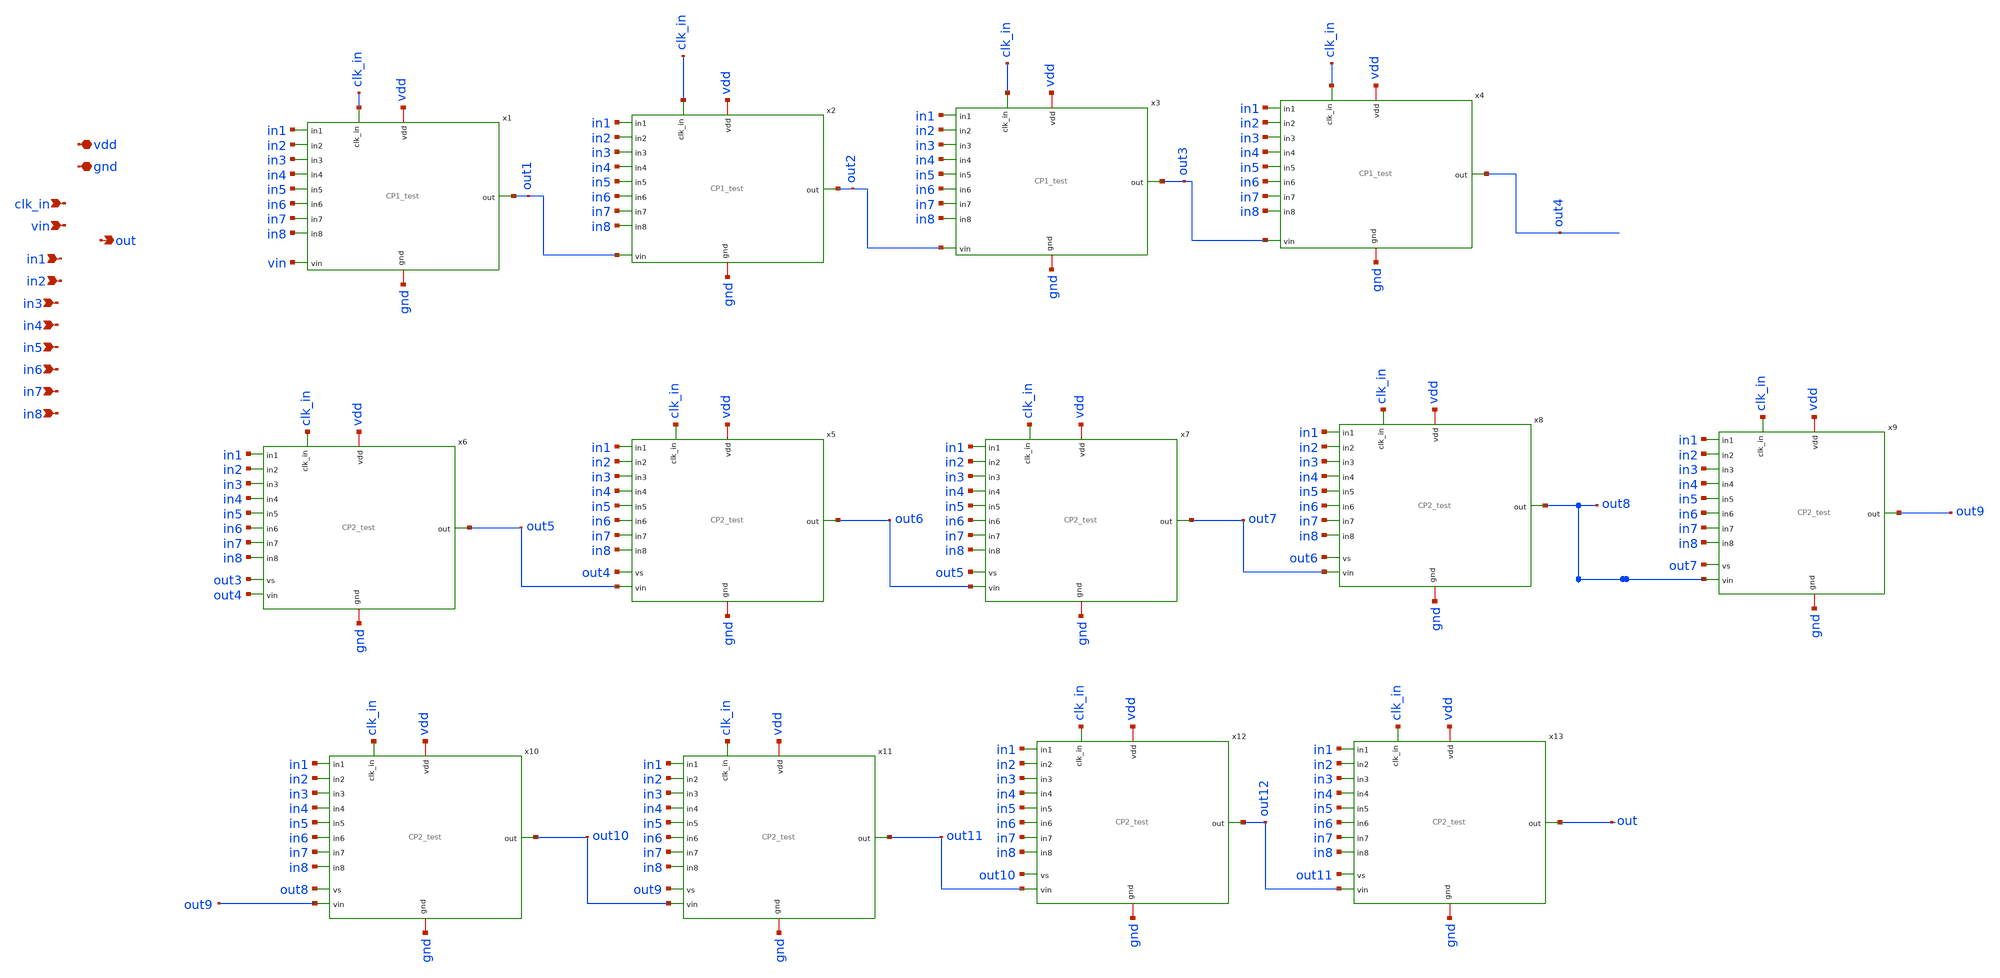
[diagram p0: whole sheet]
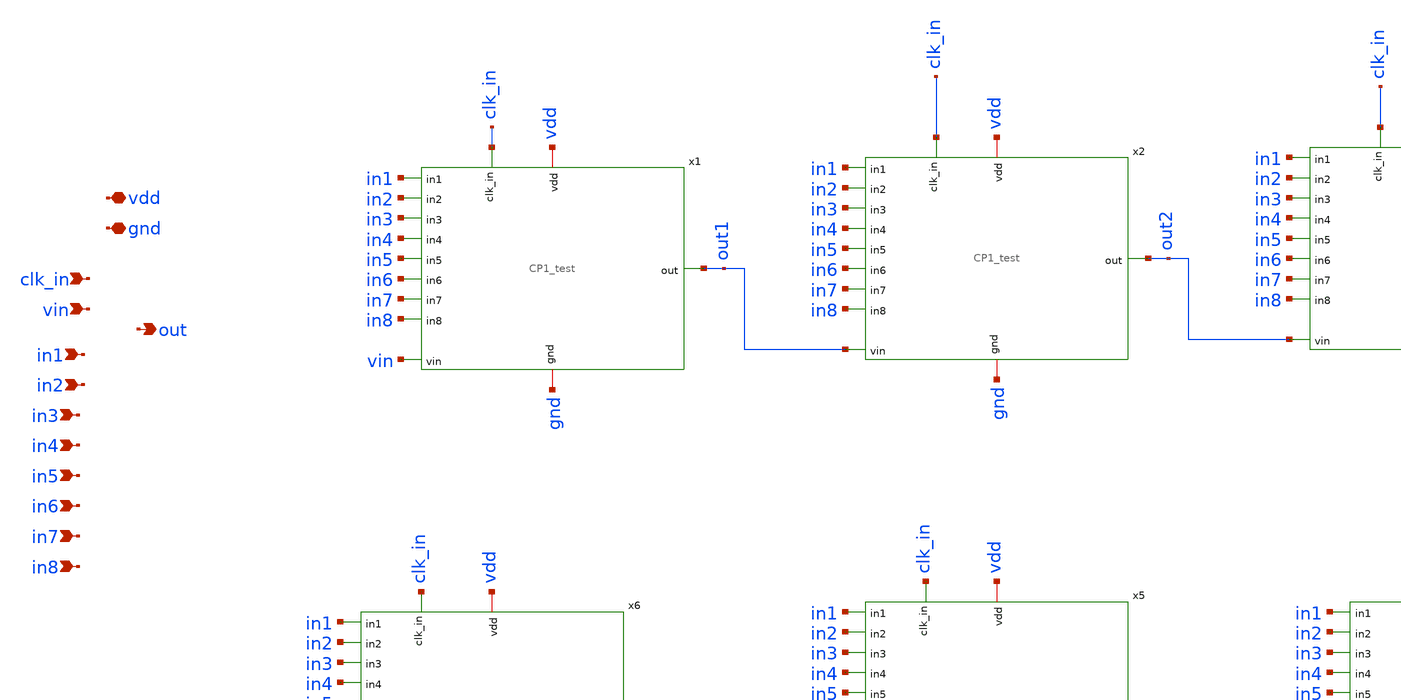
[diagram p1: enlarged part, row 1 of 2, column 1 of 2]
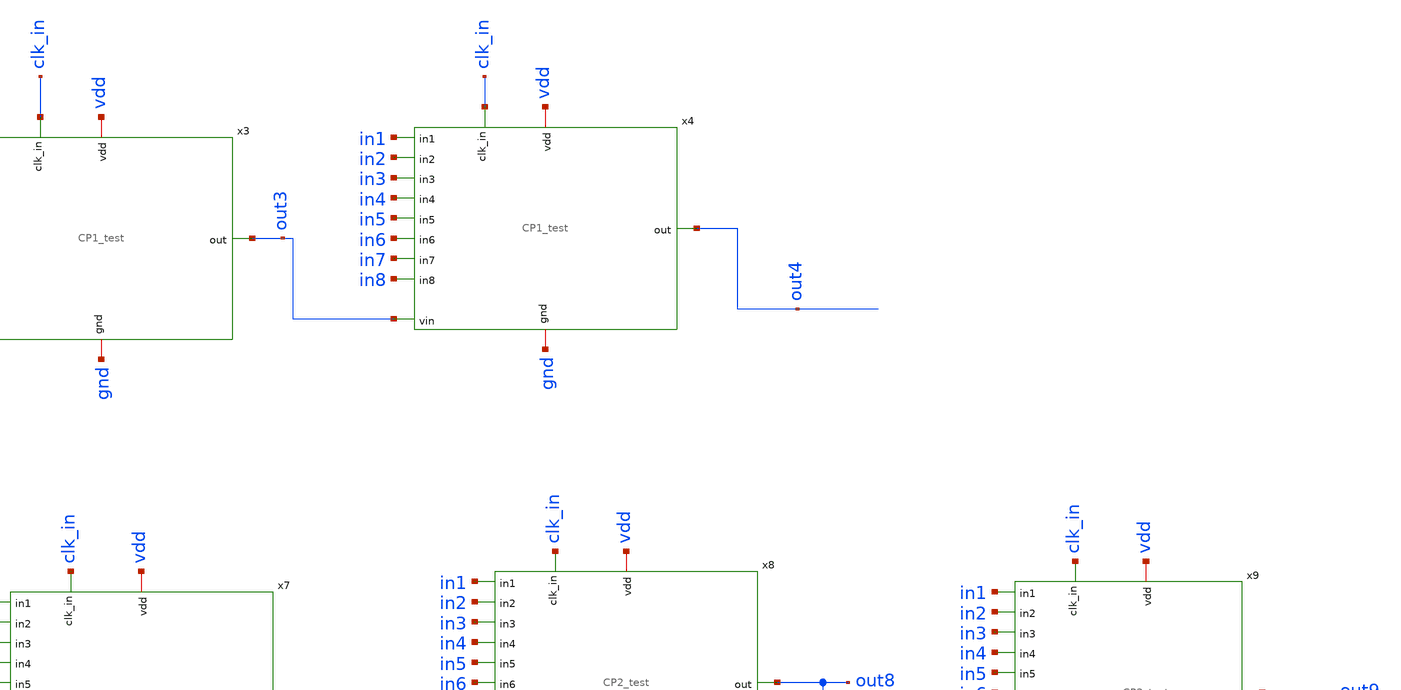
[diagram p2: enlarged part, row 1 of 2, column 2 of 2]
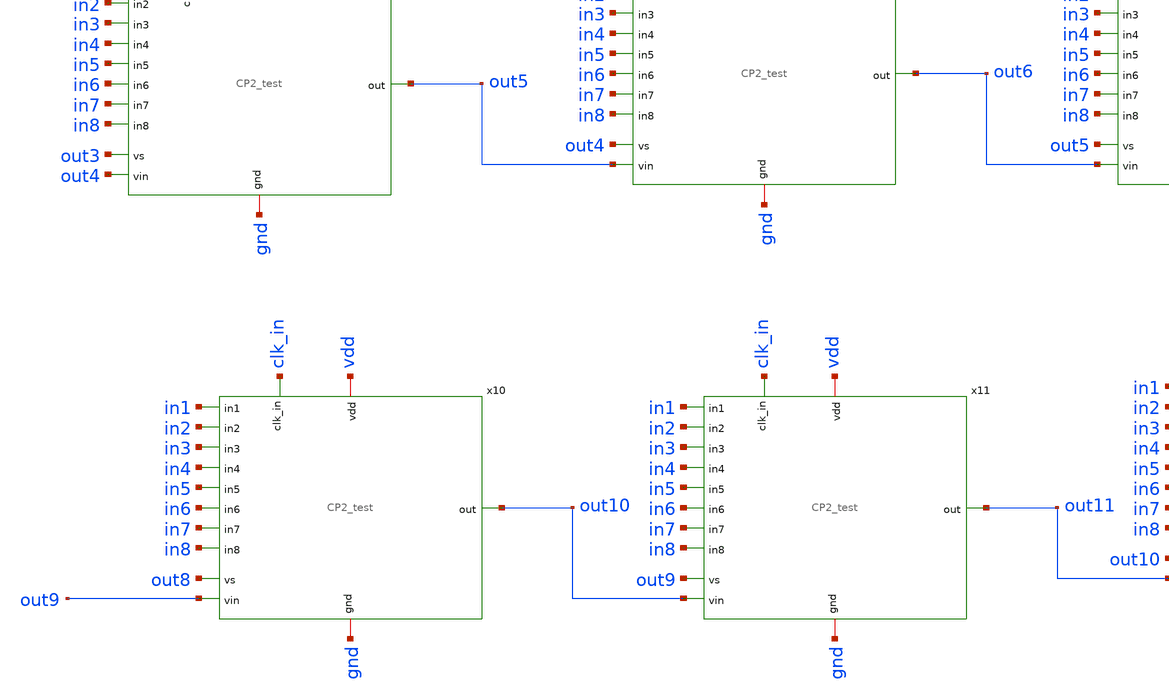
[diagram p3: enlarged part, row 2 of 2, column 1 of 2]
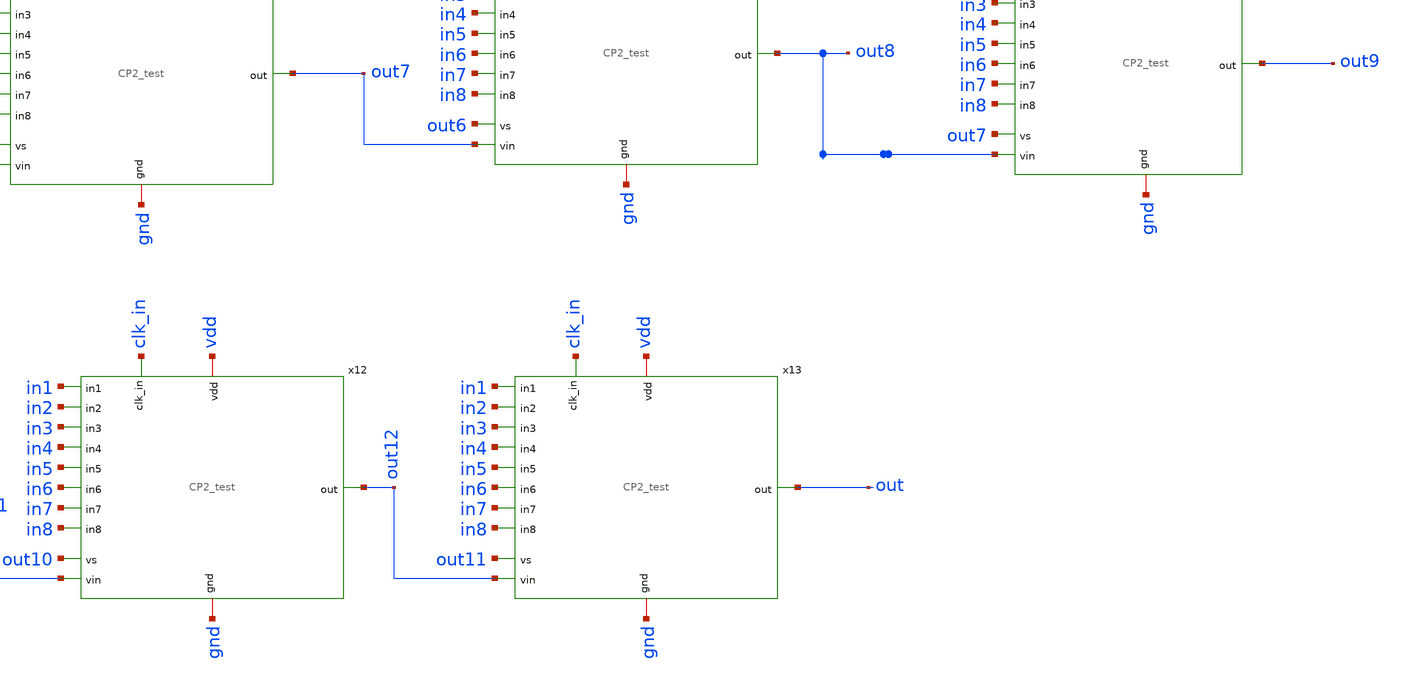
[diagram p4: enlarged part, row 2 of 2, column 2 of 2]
** sch_path: xschem/charge_pumps2/reconfigurable_CP.sch
**.subckt reconfigurable_CP clk_in gnd vdd out vin in1 in2 in3 in4 in5 in6 in7 in8
*.ipin clk_in
*.iopin gnd
*.iopin vdd
*.opin out
*.ipin vin
*.ipin in1
*.ipin in2
*.ipin in3
*.ipin in4
*.ipin in5
*.ipin in6
*.ipin in7
*.ipin in8
x1 gnd clk_in vin out1 in1 in2 in3 in4 in5 in6 in7 in8 vdd CP1_test
x2 gnd clk_in out1 out2 in1 in2 in3 in4 in5 in6 in7 in8 vdd CP1_test
x3 gnd clk_in out2 out3 in1 in2 in3 in4 in5 in6 in7 in8 vdd CP1_test
x4 gnd clk_in out3 out4 in1 in2 in3 in4 in5 in6 in7 in8 vdd CP1_test
x6 gnd out3 clk_in out4 out5 in1 in2 in3 in4 in5 in6 in7 in8 vdd CP2_test
x5 gnd out4 clk_in out5 out6 in1 in2 in3 in4 in5 in6 in7 in8 vdd CP2_test
x7 gnd out5 clk_in out6 out7 in1 in2 in3 in4 in5 in6 in7 in8 vdd CP2_test
x8 gnd out6 clk_in out7 out8 in1 in2 in3 in4 in5 in6 in7 in8 vdd CP2_test
x10 gnd out8 clk_in out9 out10 in1 in2 in3 in4 in5 in6 in7 in8 vdd CP2_test
x11 gnd out9 clk_in out10 out11 in1 in2 in3 in4 in5 in6 in7 in8 vdd CP2_test
x12 gnd out10 clk_in out11 out12 in1 in2 in3 in4 in5 in6 in7 in8 vdd CP2_test
x13 gnd out11 clk_in out12 out in1 in2 in3 in4 in5 in6 in7 in8 vdd CP2_test
x9 gnd out7 clk_in out8 out9 in1 in2 in3 in4 in5 in6 in7 in8 vdd CP2_test
**.ends
.end
